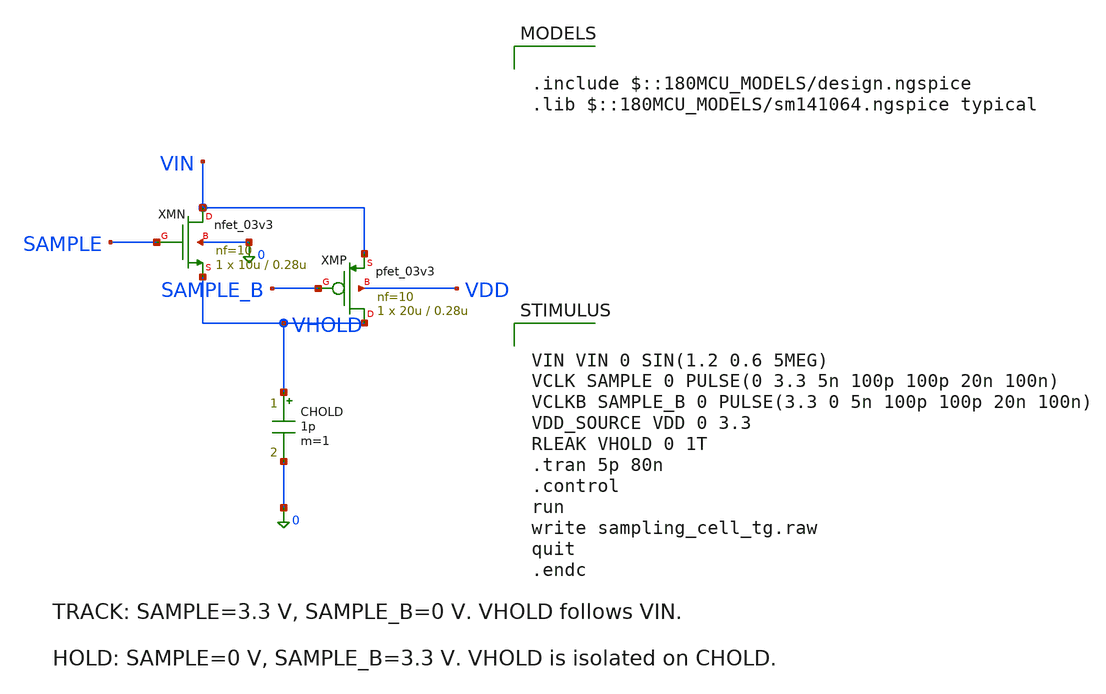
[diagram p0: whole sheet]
** sch_path: simulations/gf180_sampling_cell/sampling_cell_tg.sch
**.subckt sampling_cell_tg
XMN VIN SAMPLE VHOLD 0 nfet_03v3 L=0.28u W=10u nf=10 ad='int((nf+1)/2) * W/nf * 0.18u' as='int((nf+2)/2) * W/nf * 0.18u'
+ pd='2*int((nf+1)/2) * (W/nf + 0.18u)' ps='2*int((nf+2)/2) * (W/nf + 0.18u)' nrd='0.18u / W' nrs='0.18u / W'
+ sa=0 sb=0 sd=0 m=1
XMP VHOLD SAMPLE_B VIN VDD pfet_03v3 L=0.28u W=20u nf=10 ad='int((nf+1)/2) * W/nf * 0.18u' as='int((nf+2)/2) * W/nf * 0.18u'
+ pd='2*int((nf+1)/2) * (W/nf + 0.18u)' ps='2*int((nf+2)/2) * (W/nf + 0.18u)' nrd='0.18u / W' nrs='0.18u / W'
+ sa=0 sb=0 sd=0 m=1
CHOLD VHOLD 0 1p m=1
**** begin user architecture code

.include $::180MCU_MODELS/design.ngspice
.lib $::180MCU_MODELS/sm141064.ngspice typical



VIN VIN 0 SIN(1.2 0.6 5MEG)
VCLK SAMPLE 0 PULSE(0 3.3 5n 100p 100p 20n 100n)
VCLKB SAMPLE_B 0 PULSE(3.3 0 5n 100p 100p 20n 100n)
VDD_SOURCE VDD 0 3.3
RLEAK VHOLD 0 1T
.tran 5p 80n
.control
run
write sampling_cell_tg.raw
quit
.endc


**** end user architecture code
**.ends
.end
